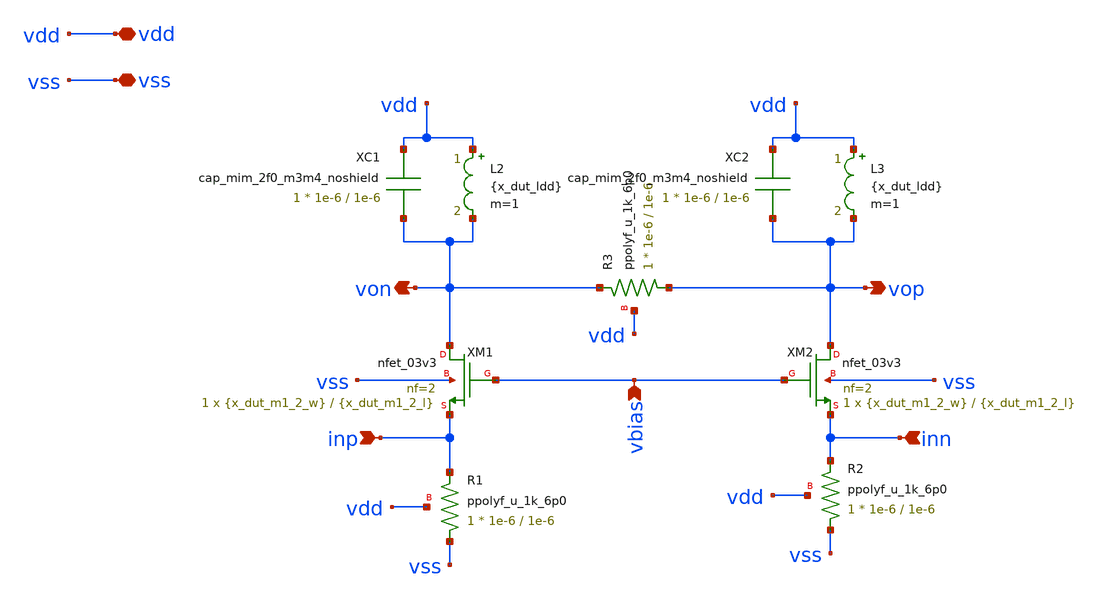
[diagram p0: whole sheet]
** sch_path: examples/tunable-tia/gf180/tia-bpf-1/bpf-tia-1-all-pdk.sch
**.subckt bpf-tia-1-all-pdk vdd vss inp inn von vop vbias
*.iopin vdd
*.iopin vss
*.ipin inp
*.ipin inn
*.opin von
*.opin vop
*.ipin vbias
XM1 von vbias inp vss nfet_03v3 L={x_dut_m1_2_l} W={x_dut_m1_2_w} nf=2 ad='int((nf+1)/2) * W/nf * 0.18u'
+ as='int((nf+2)/2) * W/nf * 0.18u' pd='2*int((nf+1)/2) * (W/nf + 0.18u)' ps='2*int((nf+2)/2) * (W/nf + 0.18u)'
+ nrd='0.18u / W' nrs='0.18u / W' sa=0 sb=0 sd=0 m=1
XM2 vop vbias inn vss nfet_03v3 L={x_dut_m1_2_l} W={x_dut_m1_2_w} nf=2 ad='int((nf+1)/2) * W/nf * 0.18u'
+ as='int((nf+2)/2) * W/nf * 0.18u' pd='2*int((nf+1)/2) * (W/nf + 0.18u)' ps='2*int((nf+2)/2) * (W/nf + 0.18u)'
+ nrd='0.18u / W' nrs='0.18u / W' sa=0 sb=0 sd=0 m=1
L2 vdd von {x_dut_ldd} m=1
L3 vdd vop {x_dut_ldd} m=1
XR1 vss inp vdd ppolyf_u_1k_6p0 r_width=1e-6 r_length=1e-6 m=1
XR2 vss inn vdd ppolyf_u_1k_6p0 r_width=1e-6 r_length=1e-6 m=1
XR3 vop von vdd ppolyf_u_1k_6p0 r_width=1e-6 r_length=1e-6 m=1
XC1 vdd von cap_mim_2f0_m3m4_noshield c_width=1e-6 c_length=1e-6 m=1
XC2 vdd vop cap_mim_2f0_m3m4_noshield c_width=1e-6 c_length=1e-6 m=1
**.ends
.end
